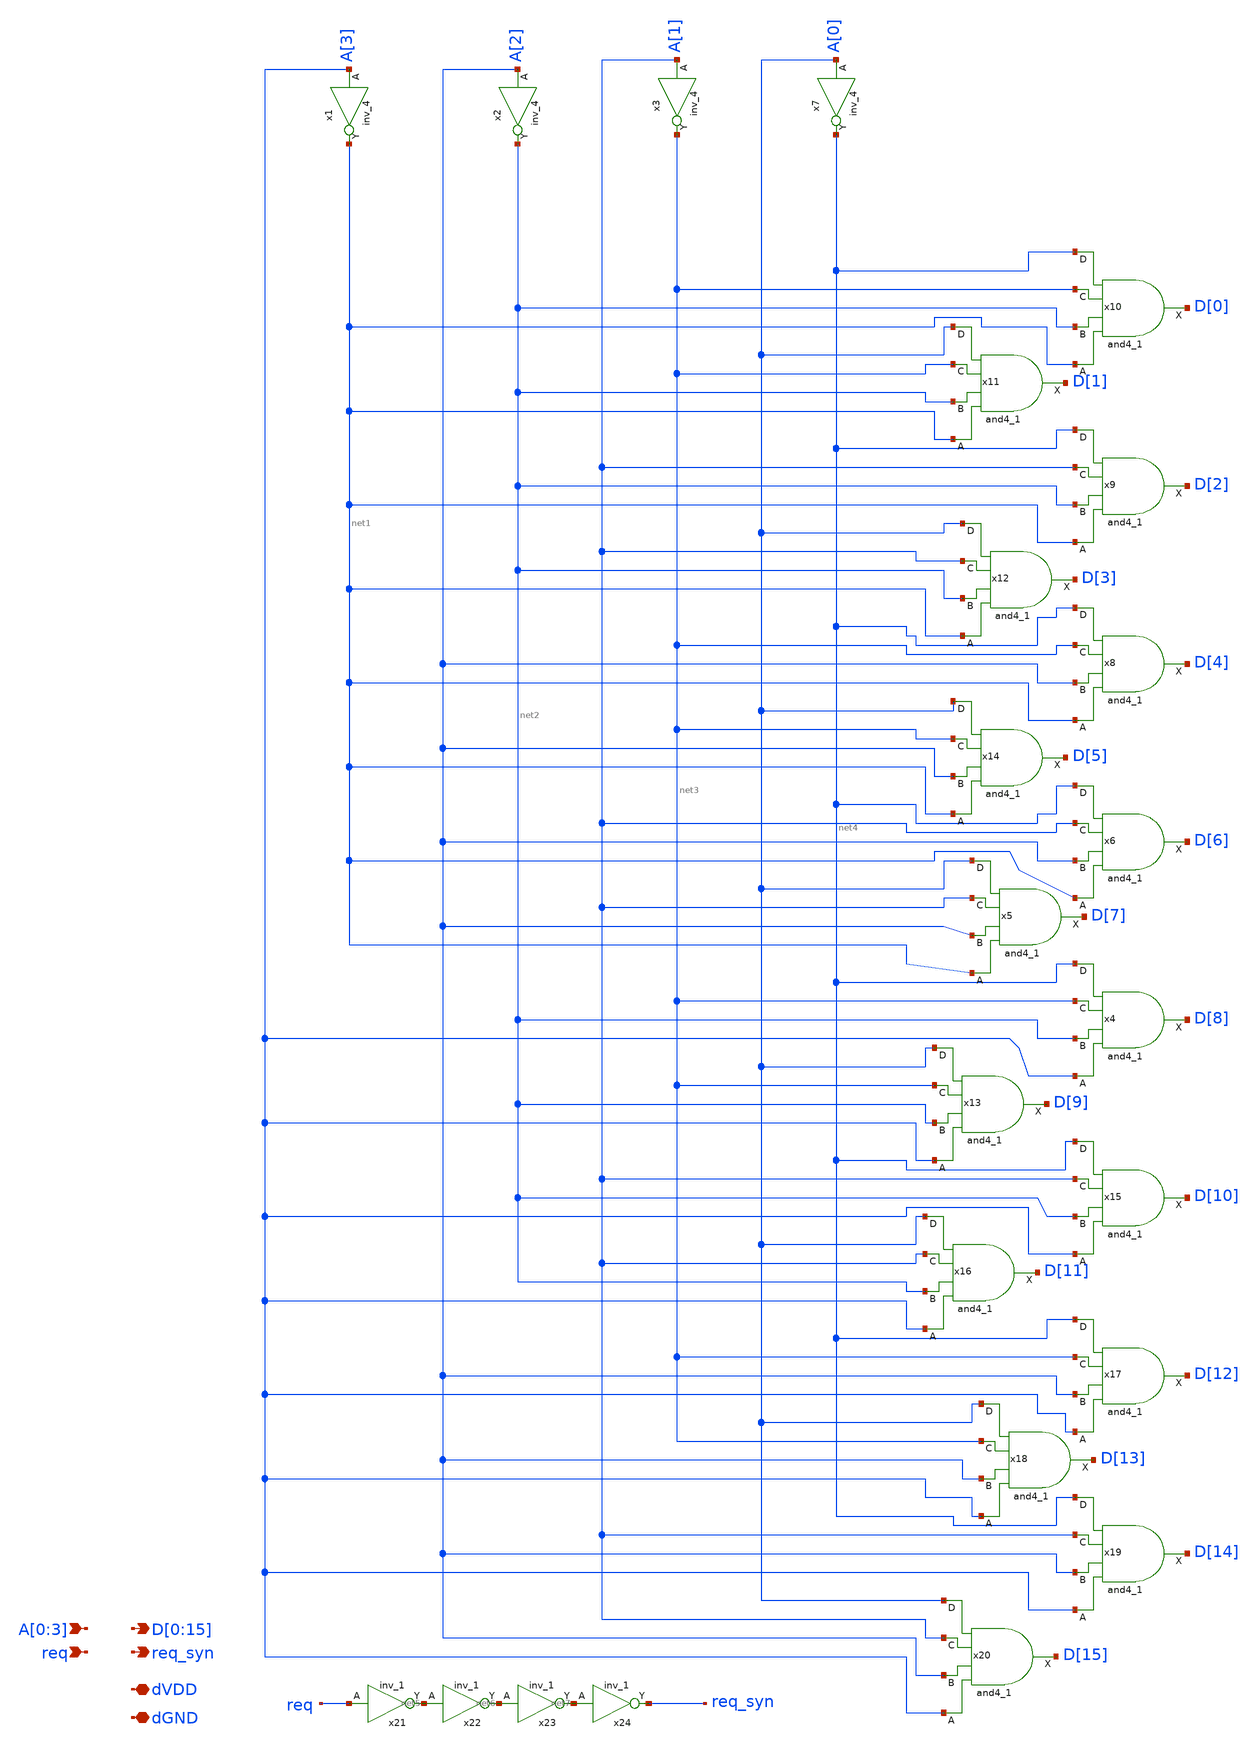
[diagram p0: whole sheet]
** sch_path: design/xschem/decoder_4_to_16.sch
**.subckt decoder_4_to_16 A[0],A[1],A[2],A[3] req
*+ D[0],D[1],D[2],D[3],D[4],D[5],D[6],D[7],D[8],D[9],D[10],D[11],D[12],D[13],D[14],D[15] req_syn dVDD dGND
*.ipin A[0],A[1],A[2],A[3]
*.ipin req
*.opin D[0],D[1],D[2],D[3],D[4],D[5],D[6],D[7],D[8],D[9],D[10],D[11],D[12],D[13],D[14],D[15]
*.opin req_syn
*.iopin dVDD
*.iopin dGND
x21 req dGND dGND dVDD dVDD net5 sky130_fd_sc_hd__inv_1
x22 net5 dGND dGND dVDD dVDD net6 sky130_fd_sc_hd__inv_1
x23 net6 dGND dGND dVDD dVDD net7 sky130_fd_sc_hd__inv_1
x24 net7 dGND dGND dVDD dVDD req_syn sky130_fd_sc_hd__inv_1
x20 A[3] A[2] A[1] A[0] dGND dGND dVDD dVDD D[15] sky130_fd_sc_hd__and4_1
x19 A[3] A[2] A[1] net4 dGND dGND dVDD dVDD D[14] sky130_fd_sc_hd__and4_1
x18 A[3] A[2] net3 A[0] dGND dGND dVDD dVDD D[13] sky130_fd_sc_hd__and4_1
x17 A[3] A[2] net3 net4 dGND dGND dVDD dVDD D[12] sky130_fd_sc_hd__and4_1
x16 A[3] net2 A[1] A[0] dGND dGND dVDD dVDD D[11] sky130_fd_sc_hd__and4_1
x15 A[3] net2 A[1] net4 dGND dGND dVDD dVDD D[10] sky130_fd_sc_hd__and4_1
x13 A[3] net2 net3 A[0] dGND dGND dVDD dVDD D[9] sky130_fd_sc_hd__and4_1
x4 A[3] net2 net3 net4 dGND dGND dVDD dVDD D[8] sky130_fd_sc_hd__and4_1
x5 net1 A[2] A[1] A[0] dGND dGND dVDD dVDD D[7] sky130_fd_sc_hd__and4_1
x6 net1 A[2] A[1] net4 dGND dGND dVDD dVDD D[6] sky130_fd_sc_hd__and4_1
x8 net1 A[2] net3 net4 dGND dGND dVDD dVDD D[4] sky130_fd_sc_hd__and4_1
x9 net1 net2 A[1] net4 dGND dGND dVDD dVDD D[2] sky130_fd_sc_hd__and4_1
x10 net1 net2 net3 net4 dGND dGND dVDD dVDD D[0] sky130_fd_sc_hd__and4_1
x11 net1 net2 net3 A[0] dGND dGND dVDD dVDD D[1] sky130_fd_sc_hd__and4_1
x12 net1 net2 A[1] A[0] dGND dGND dVDD dVDD D[3] sky130_fd_sc_hd__and4_1
x14 net1 A[2] net3 A[0] dGND dGND dVDD dVDD D[5] sky130_fd_sc_hd__and4_1
x1 A[3] dGND dGND dVDD dVDD net1 sky130_fd_sc_hd__inv_4
x2 A[2] dGND dGND dVDD dVDD net2 sky130_fd_sc_hd__inv_4
x3 A[1] dGND dGND dVDD dVDD net3 sky130_fd_sc_hd__inv_4
x7 A[0] dGND dGND dVDD dVDD net4 sky130_fd_sc_hd__inv_4
**.ends
.end
